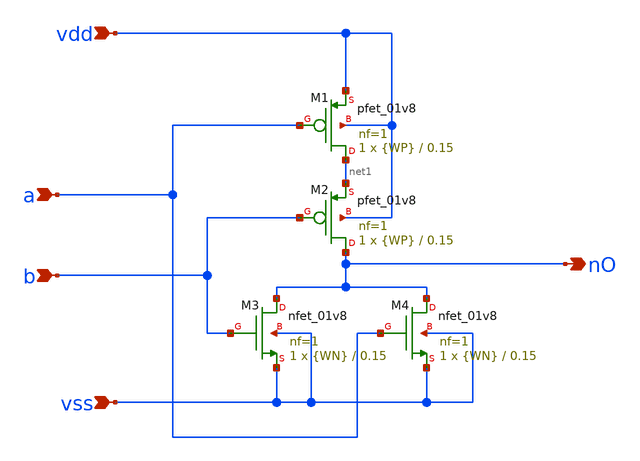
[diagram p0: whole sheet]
** sch_path: eamta2021/sch/nor/nor.sch
**.subckt nor vdd a b vss nO
*.ipin vdd
*.ipin a
*.ipin b
*.ipin vss
*.opin nO
XM1 net1 a vdd vdd sky130_fd_pr__pfet_01v8 L=0.15 W={WP} nf=1 ad='int((nf+1)/2) * W/nf * 0.29' as='int((nf+2)/2) * W/nf * 0.29'
+ pd='2*int((nf+1)/2) * (W/nf + 0.29)' ps='2*int((nf+2)/2) * (W/nf + 0.29)' nrd='0.29 / W' nrs='0.29 / W'
+ sa=0 sb=0 sd=0 mult=1 m=1
XM2 nO b net1 vdd sky130_fd_pr__pfet_01v8 L=0.15 W={WP} nf=1 ad='int((nf+1)/2) * W/nf * 0.29' as='int((nf+2)/2) * W/nf * 0.29'
+ pd='2*int((nf+1)/2) * (W/nf + 0.29)' ps='2*int((nf+2)/2) * (W/nf + 0.29)' nrd='0.29 / W' nrs='0.29 / W'
+ sa=0 sb=0 sd=0 mult=1 m=1
XM3 nO b vss vss sky130_fd_pr__nfet_01v8 L=0.15 W={WN} nf=1 ad='int((nf+1)/2) * W/nf * 0.29' as='int((nf+2)/2) * W/nf * 0.29'
+ pd='2*int((nf+1)/2) * (W/nf + 0.29)' ps='2*int((nf+2)/2) * (W/nf + 0.29)' nrd='0.29 / W' nrs='0.29 / W'
+ sa=0 sb=0 sd=0 mult=1 m=1
XM4 nO a vss vss sky130_fd_pr__nfet_01v8 L=0.15 W={WN} nf=1 ad='int((nf+1)/2) * W/nf * 0.29' as='int((nf+2)/2) * W/nf * 0.29'
+ pd='2*int((nf+1)/2) * (W/nf + 0.29)' ps='2*int((nf+2)/2) * (W/nf + 0.29)' nrd='0.29 / W' nrs='0.29 / W'
+ sa=0 sb=0 sd=0 mult=1 m=1
**.ends
.end
